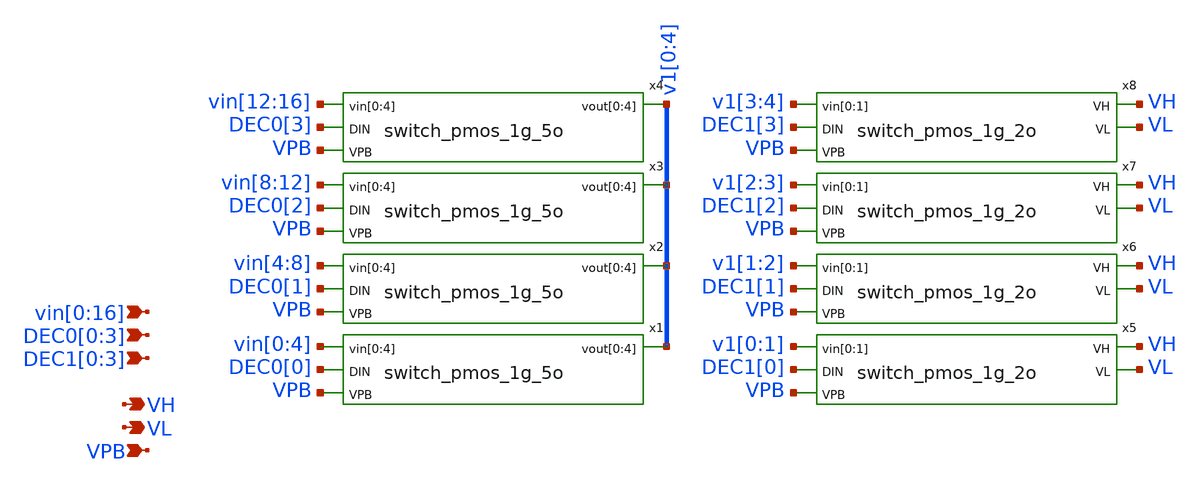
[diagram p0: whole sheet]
** sch_path: xschem/vselector_4b_2v_v2.sch
**.subckt vselector_4b_2v_v2
*+ vin[0],vin[1],vin[2],vin[3],vin[4],vin[5],vin[6],vin[7],vin[8],vin[9],vin[10],vin[11],vin[12],vin[13],vin[14],vin[15],vin[16] VH VPB DEC0[0],DEC0[1],DEC0[2],DEC0[3] VL DEC1[0],DEC1[1],DEC1[2],DEC1[3]
*.ipin
*+ vin[0],vin[1],vin[2],vin[3],vin[4],vin[5],vin[6],vin[7],vin[8],vin[9],vin[10],vin[11],vin[12],vin[13],vin[14],vin[15],vin[16]
*.opin VH
*.ipin VPB
*.ipin DEC0[0],DEC0[1],DEC0[2],DEC0[3]
*.opin VL
*.ipin DEC1[0],DEC1[1],DEC1[2],DEC1[3]
x1 vin[0] vin[1] vin[2] vin[3] vin[4] DEC0[0] v1[0] v1[1] v1[2] v1[3] v1[4] VPB switch_pmos_1g_5o
x2 vin[4] vin[5] vin[6] vin[7] vin[8] DEC0[1] v1[0] v1[1] v1[2] v1[3] v1[4] VPB switch_pmos_1g_5o
x3 vin[8] vin[9] vin[10] vin[11] vin[12] DEC0[2] v1[0] v1[1] v1[2] v1[3] v1[4] VPB switch_pmos_1g_5o
x4 vin[12] vin[13] vin[14] vin[15] vin[16] DEC0[3] v1[0] v1[1] v1[2] v1[3] v1[4] VPB
+ switch_pmos_1g_5o
x5 v1[0] v1[1] DEC1[0] VH VL VPB switch_pmos_1g_2o
x6 v1[1] v1[2] DEC1[1] VH VL VPB switch_pmos_1g_2o
x7 v1[2] v1[3] DEC1[2] VH VL VPB switch_pmos_1g_2o
x8 v1[3] v1[4] DEC1[3] VH VL VPB switch_pmos_1g_2o
**.ends

* expanding   symbol:  switch_pmos_1g_5o.sym # of pins=4
** sym_path: xschem/switch_pmos_1g_5o.sym
** sch_path: xschem/switch_pmos_1g_5o.sch
.subckt switch_pmos_1g_5o vin[0] vin[1] vin[2] vin[3] vin[4] DIN vout[0] vout[1] vout[2] vout[3]
+ vout[4] VPB
*.ipin vin[0],vin[1],vin[2],vin[3],vin[4]
*.opin vout[0],vout[1],vout[2],vout[3],vout[4]
*.ipin VPB
*.ipin DIN
.param wp=0.42 wn=0.42 l=0.5

XM1 vout[0] DIN vin[0] VPB sky130_fd_pr__pfet_g5v0d10v5 L=l W=wp nf=1 ad='int((nf+1)/2) * W/nf * 0.29'
+ as='int((nf+2)/2) * W/nf * 0.29' pd='2*int((nf+1)/2) * (W/nf + 0.29)' ps='2*int((nf+2)/2) * (W/nf + 0.29)'
+ nrd='0.29 / W' nrs='0.29 / W' sa=0 sb=0 sd=0 mult=1 m=1
XM2 vout[1] DIN vin[1] VPB sky130_fd_pr__pfet_g5v0d10v5 L=l W=wp nf=1 ad='int((nf+1)/2) * W/nf * 0.29'
+ as='int((nf+2)/2) * W/nf * 0.29' pd='2*int((nf+1)/2) * (W/nf + 0.29)' ps='2*int((nf+2)/2) * (W/nf + 0.29)'
+ nrd='0.29 / W' nrs='0.29 / W' sa=0 sb=0 sd=0 mult=1 m=1
XM3 vout[2] DIN vin[2] VPB sky130_fd_pr__pfet_g5v0d10v5 L=l W=wp nf=1 ad='int((nf+1)/2) * W/nf * 0.29'
+ as='int((nf+2)/2) * W/nf * 0.29' pd='2*int((nf+1)/2) * (W/nf + 0.29)' ps='2*int((nf+2)/2) * (W/nf + 0.29)'
+ nrd='0.29 / W' nrs='0.29 / W' sa=0 sb=0 sd=0 mult=1 m=1
XM4 vout[3] DIN vin[3] VPB sky130_fd_pr__pfet_g5v0d10v5 L=l W=wp nf=1 ad='int((nf+1)/2) * W/nf * 0.29'
+ as='int((nf+2)/2) * W/nf * 0.29' pd='2*int((nf+1)/2) * (W/nf + 0.29)' ps='2*int((nf+2)/2) * (W/nf + 0.29)'
+ nrd='0.29 / W' nrs='0.29 / W' sa=0 sb=0 sd=0 mult=1 m=1
XM5 vout[4] DIN vin[4] VPB sky130_fd_pr__pfet_g5v0d10v5 L=l W=wp nf=1 ad='int((nf+1)/2) * W/nf * 0.29'
+ as='int((nf+2)/2) * W/nf * 0.29' pd='2*int((nf+1)/2) * (W/nf + 0.29)' ps='2*int((nf+2)/2) * (W/nf + 0.29)'
+ nrd='0.29 / W' nrs='0.29 / W' sa=0 sb=0 sd=0 mult=1 m=1
.ends


* expanding   symbol:  switch_pmos_1g_2o.sym # of pins=5
** sym_path: xschem/switch_pmos_1g_2o.sym
** sch_path: xschem/switch_pmos_1g_2o.sch
.subckt switch_pmos_1g_2o vin[0] vin[1] DIN VH VL VPB
*.ipin vin[0],vin[1]
*.opin VH
*.ipin VPB
*.ipin DIN
*.opin VL
.param wp=0.42 wn=0.42 l=0.5

XM1 VL DIN vin[0] VPB sky130_fd_pr__pfet_g5v0d10v5 L=l W=wp nf=1 ad='int((nf+1)/2) * W/nf * 0.29' as='int((nf+2)/2) * W/nf * 0.29'
+ pd='2*int((nf+1)/2) * (W/nf + 0.29)' ps='2*int((nf+2)/2) * (W/nf + 0.29)' nrd='0.29 / W' nrs='0.29 / W'
+ sa=0 sb=0 sd=0 mult=1 m=1
XM2 VH DIN vin[1] VPB sky130_fd_pr__pfet_g5v0d10v5 L=l W=wp nf=1 ad='int((nf+1)/2) * W/nf * 0.29' as='int((nf+2)/2) * W/nf * 0.29'
+ pd='2*int((nf+1)/2) * (W/nf + 0.29)' ps='2*int((nf+2)/2) * (W/nf + 0.29)' nrd='0.29 / W' nrs='0.29 / W'
+ sa=0 sb=0 sd=0 mult=1 m=1
.ends

.end
